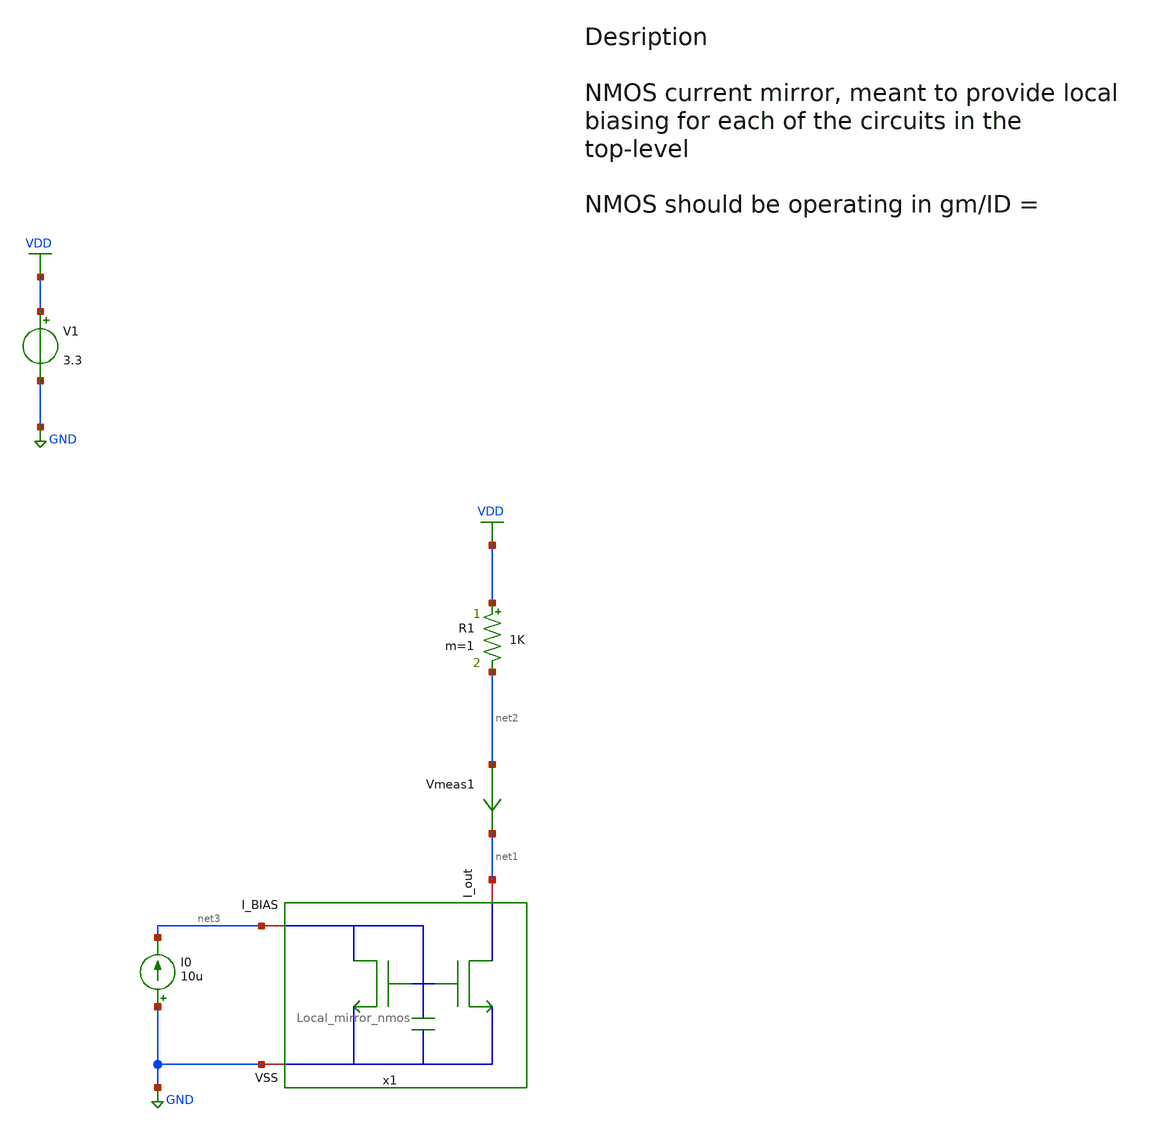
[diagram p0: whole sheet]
** sch_path: src/design_tb/Local_mirror_nmos_tb.sch
**.subckt Local_mirror_nmos_tb
I0 GND net3 10u
V1 VDD GND 3.3
.save i(v1)
Vmeas1 net2 net1 0
.save i(vmeas1)
R1 VDD net2 1K m=1
x1 net1 net3 GND Local_mirror_nmos l_ref=1u w_ref=1.5u nf_ref= l_mir=1u w_mir=7.5u nf_mir=
**** begin user architecture code

.include $::180MCU_MODELS/design.ngspice
.lib $::180MCU_MODELS/sm141064.ngspice typical
.lib $::180MCU_MODELS/sm141064.ngspice mimcap_typical
.lib $::180MCU_MODELS/sm141064.ngspice res_typical
.lib $::180MCU_MODELS/sm141064.ngspice cap_mim



* Add convergence aids
.option method=gear

.control

    * operating point
    op
    show

    write Local_mirror_nmos_tb.raw

    set appendwrite

    * Transient analysis to observe mixing operation
    tran 1n 0.01u
    write Local_mirror_nmos_tb.raw

.endc


**** end user architecture code
**.ends
.GLOBAL GND
.GLOBAL VDD
.end
